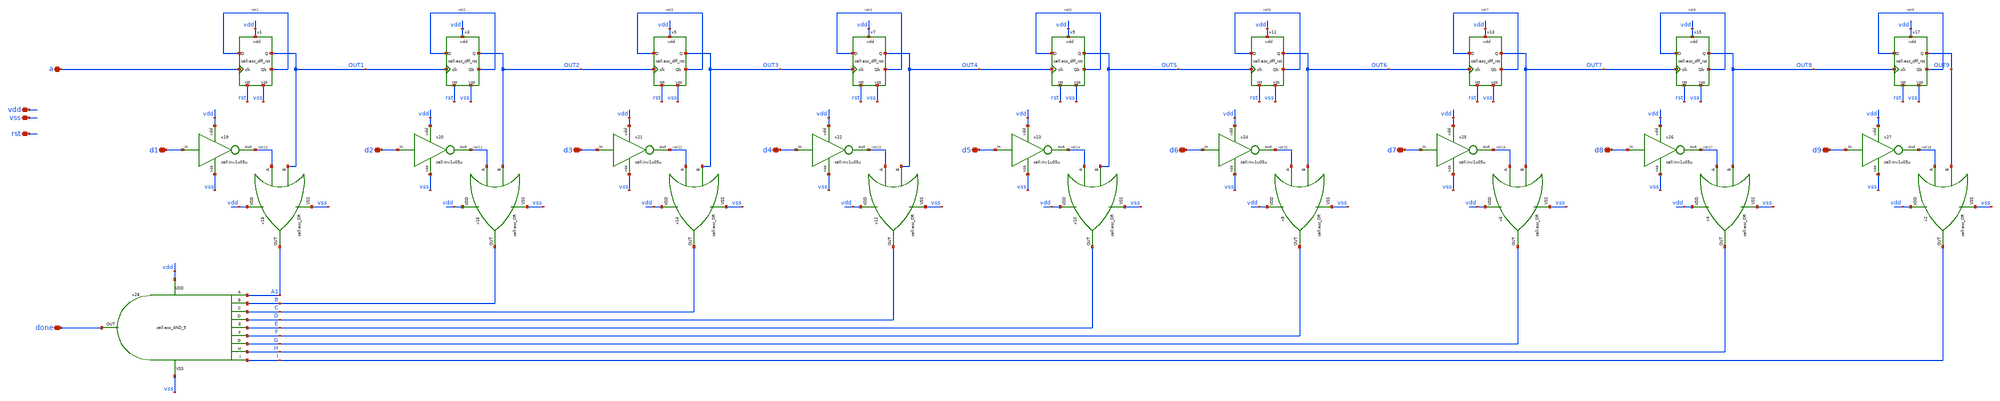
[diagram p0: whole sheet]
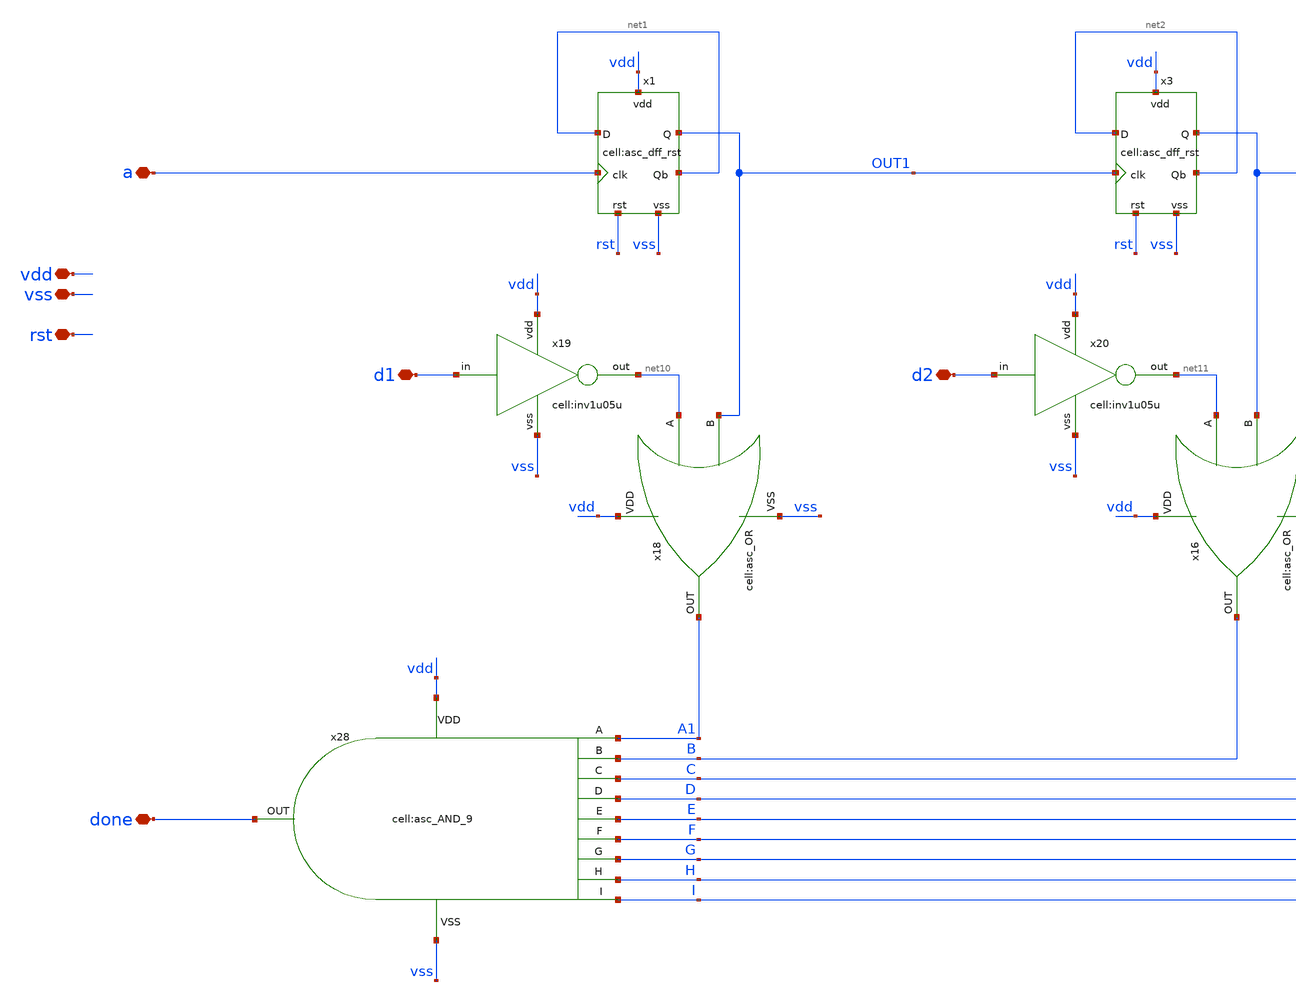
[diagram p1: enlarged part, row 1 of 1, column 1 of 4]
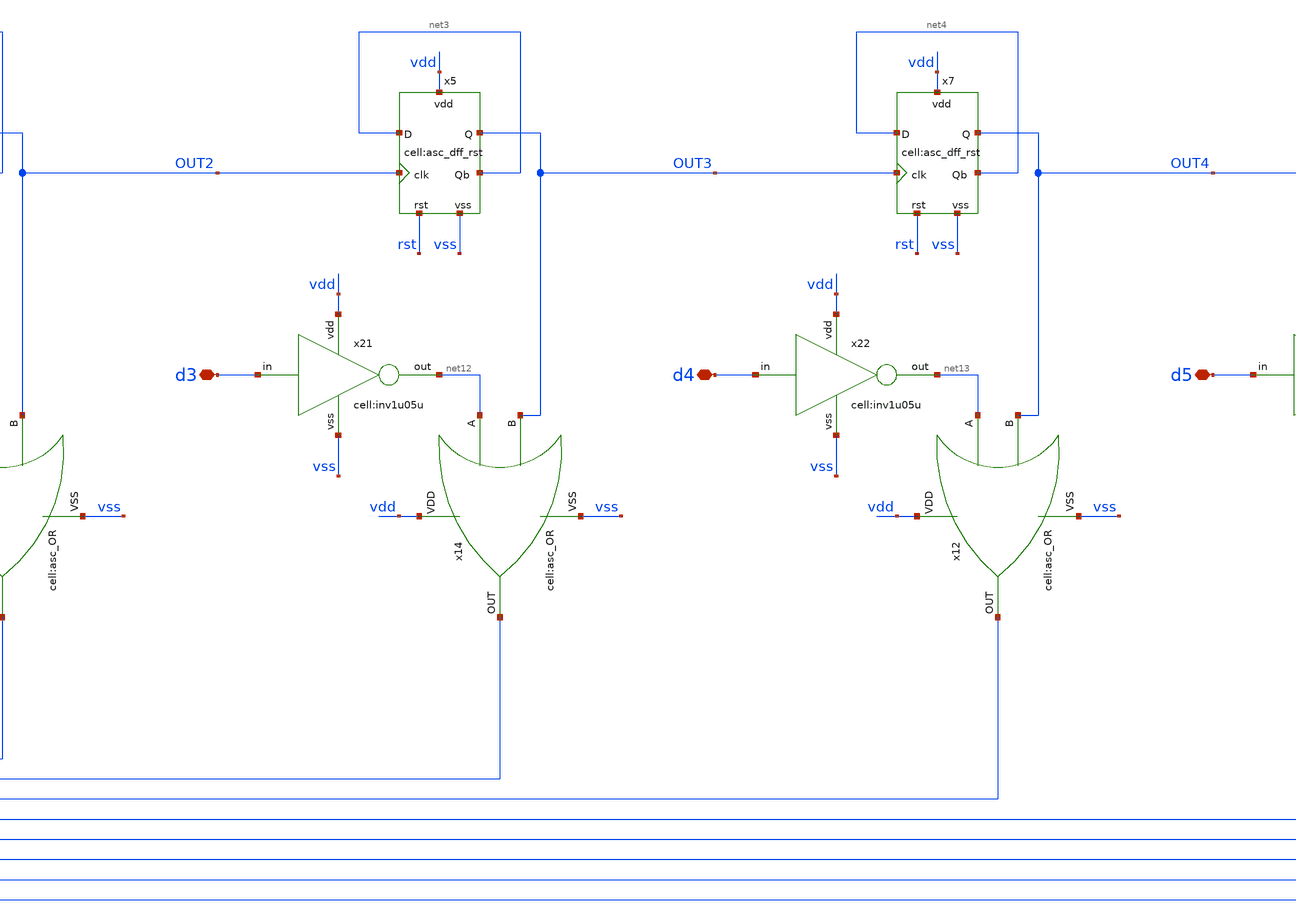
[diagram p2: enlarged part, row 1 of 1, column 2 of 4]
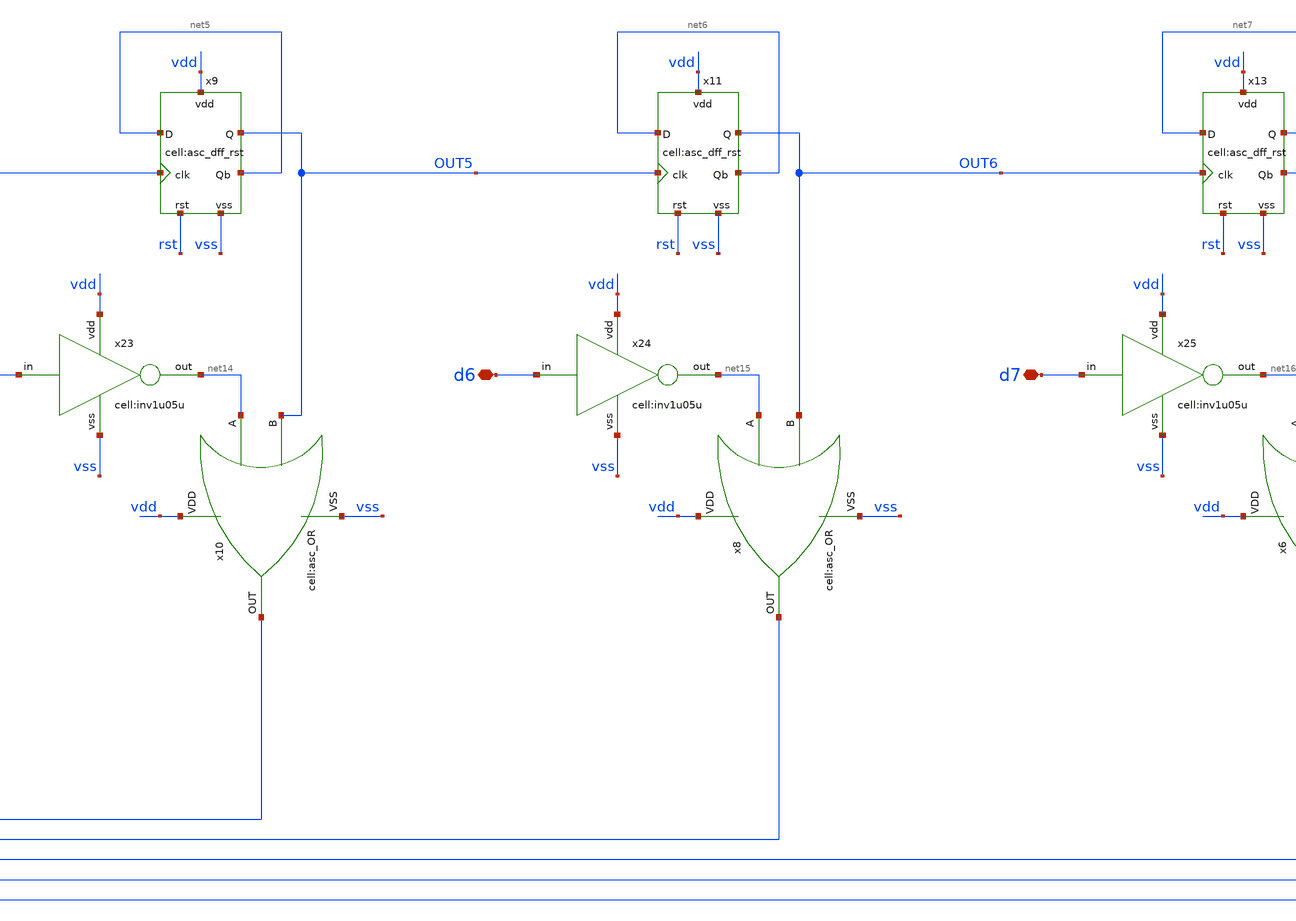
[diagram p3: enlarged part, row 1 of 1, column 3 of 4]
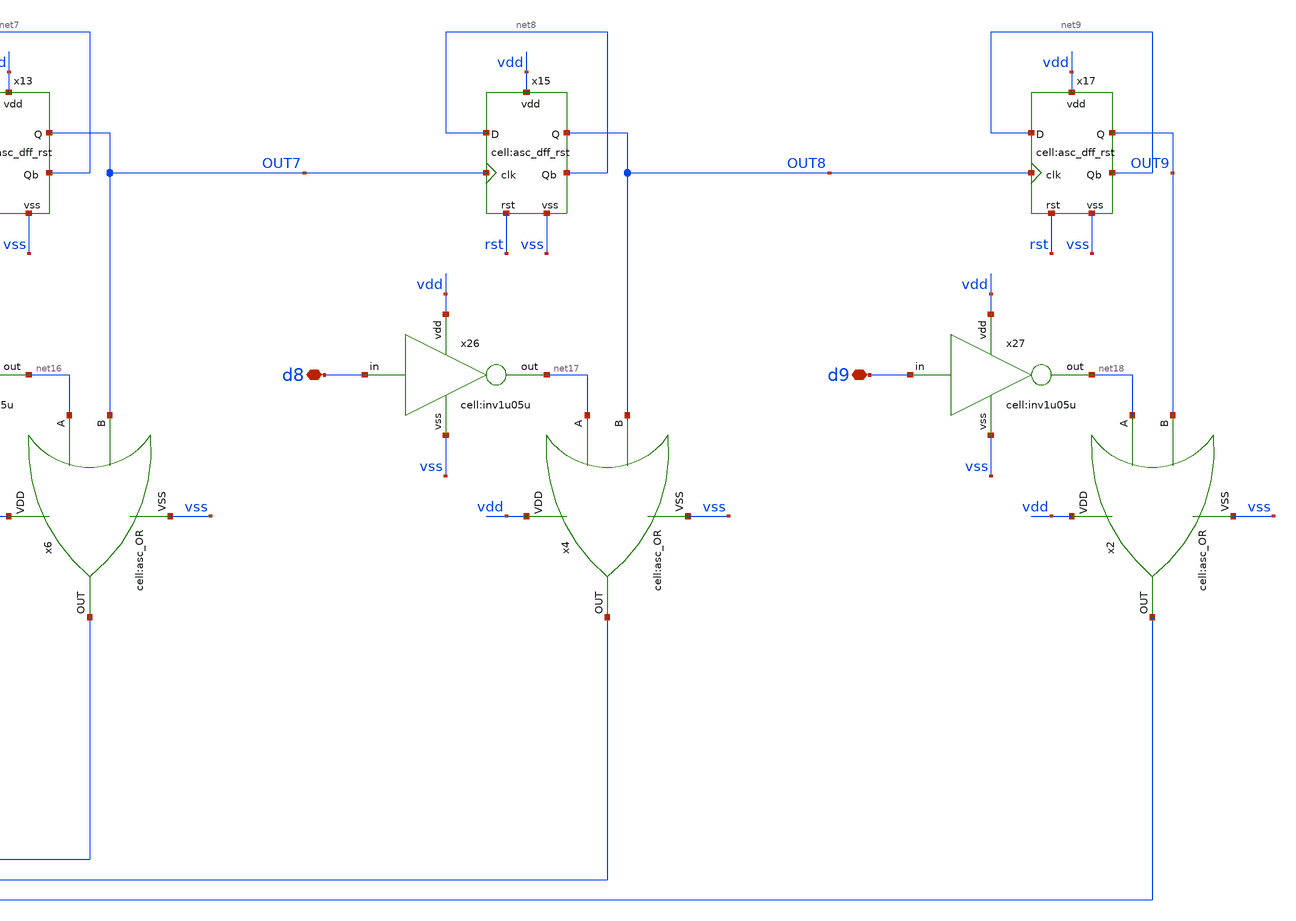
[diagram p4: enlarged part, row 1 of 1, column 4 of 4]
** sch_path: designs/libs/xp_core_analog/asc_9_bit_counter_20250721/asc_9_bit_counter_20250721.sch
**.subckt asc_9_bit_counter_20250721 a vdd vss done d1 d2 d3 d4 d5 d6 d7 d8 d9 rst
*.iopin a
*.iopin vdd
*.iopin vss
*.iopin done
*.iopin d1
*.iopin d2
*.iopin d3
*.iopin d4
*.iopin d5
*.iopin d6
*.iopin d7
*.iopin d8
*.iopin d9
*.iopin rst
x28 vdd vss done A1 B C D E F G H I asc_AND_9
x1 a net1 net1 vdd vss OUT1 rst asc_dff_rst
x3 OUT1 net2 net2 vdd vss OUT2 rst asc_dff_rst
x5 OUT2 net3 net3 vdd vss OUT3 rst asc_dff_rst
x7 OUT3 net4 net4 vdd vss OUT4 rst asc_dff_rst
x9 OUT4 net5 net5 vdd vss OUT5 rst asc_dff_rst
x11 OUT5 net6 net6 vdd vss OUT6 rst asc_dff_rst
x13 OUT6 net7 net7 vdd vss OUT7 rst asc_dff_rst
x15 OUT7 net8 net8 vdd vss OUT8 rst asc_dff_rst
x17 OUT8 net9 net9 vdd vss OUT9 rst asc_dff_rst
x2 vdd vss I net18 OUT9 asc_OR
x4 vdd vss H net17 OUT8 asc_OR
x6 vdd vss G net16 OUT7 asc_OR
x8 vdd vss F net15 OUT6 asc_OR
x10 vdd vss E net14 OUT5 asc_OR
x12 vdd vss D net13 OUT4 asc_OR
x14 vdd vss C net12 OUT3 asc_OR
x16 vdd vss B net11 OUT2 asc_OR
x18 vdd vss A1 net10 OUT1 asc_OR
x19 d1 vdd net10 vss inv1u05u
x20 d2 vdd net11 vss inv1u05u
x21 d3 vdd net12 vss inv1u05u
x22 d4 vdd net13 vss inv1u05u
x23 d5 vdd net14 vss inv1u05u
x24 d6 vdd net15 vss inv1u05u
x25 d7 vdd net16 vss inv1u05u
x26 d8 vdd net17 vss inv1u05u
x27 d9 vdd net18 vss inv1u05u
**.ends
.end
